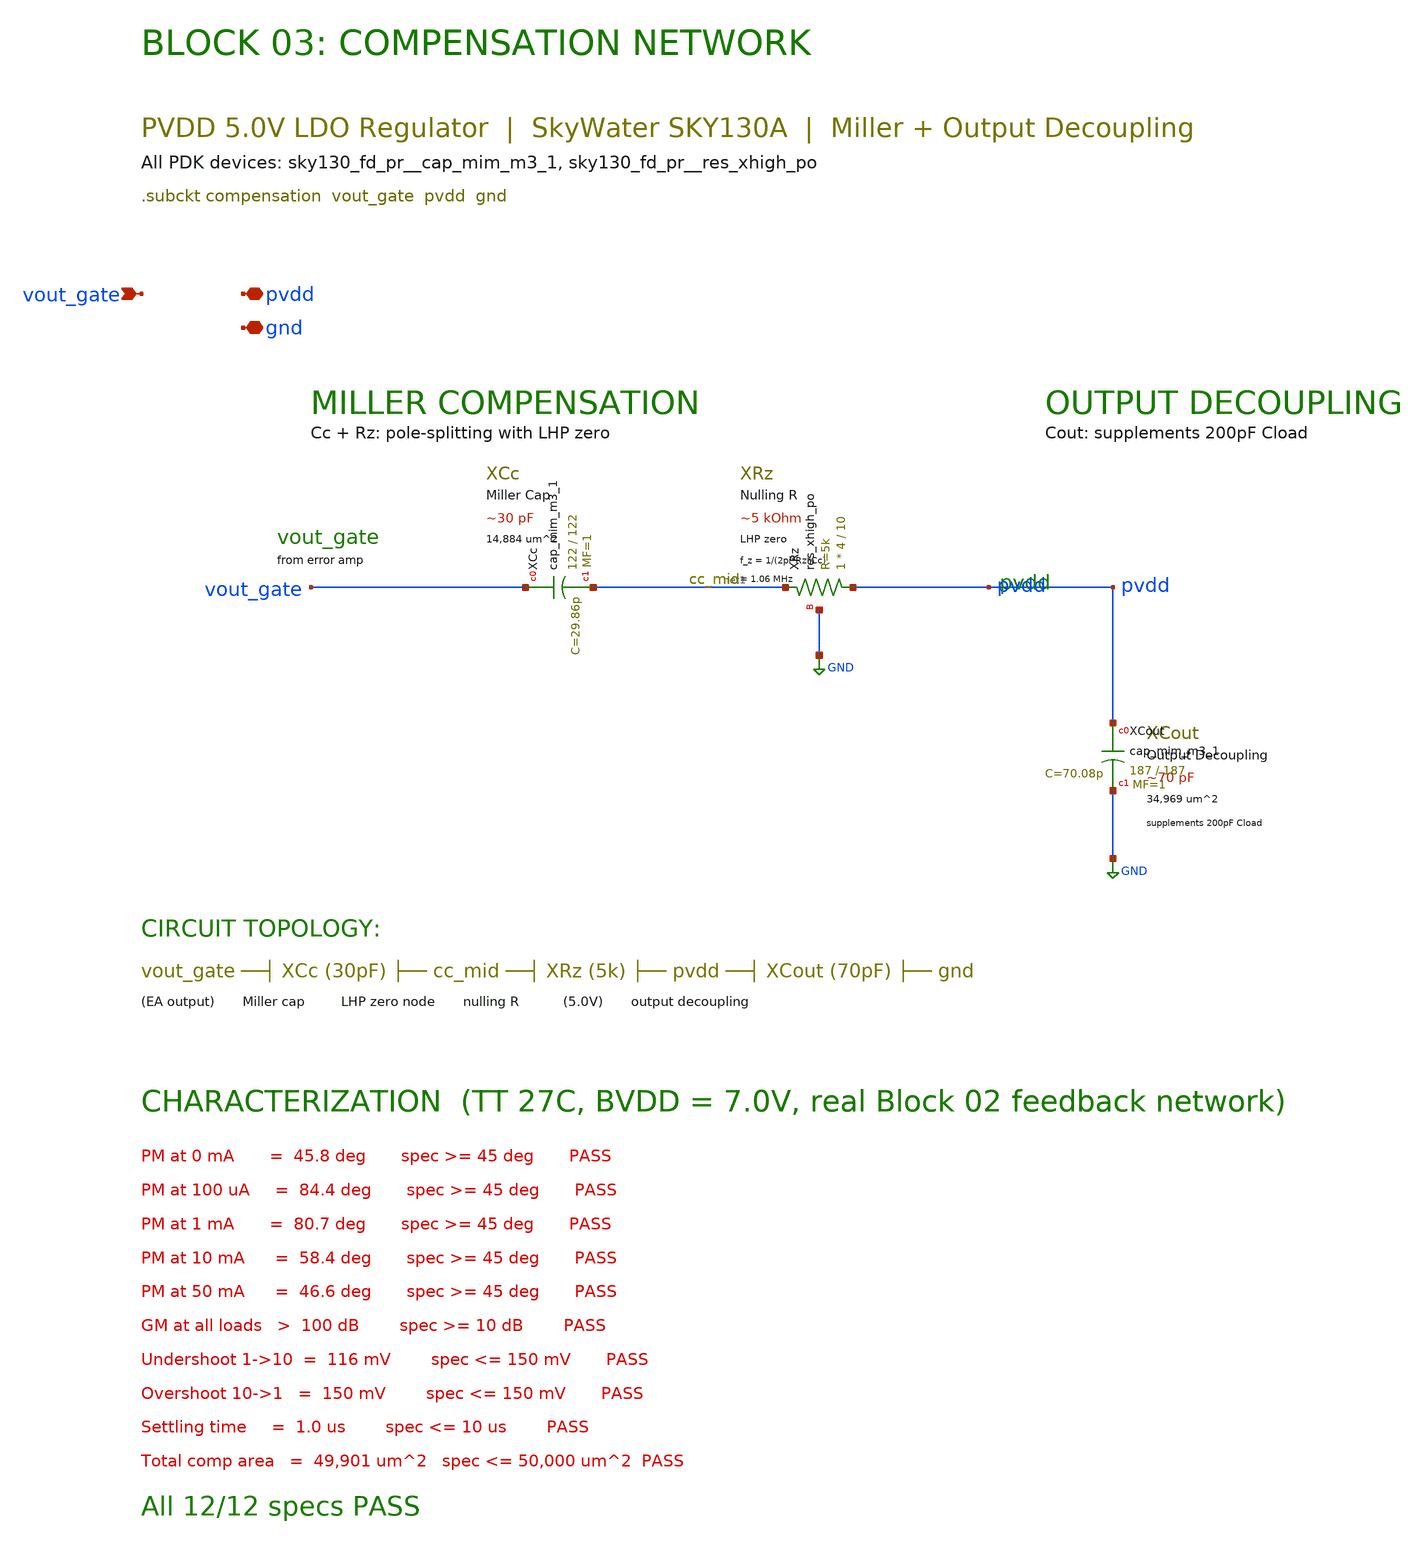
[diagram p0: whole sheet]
** sch_path: pvdd_regulator/03_compensation/compensation.sch
**.subckt compensation vout_gate pvdd gnd
*.ipin vout_gate
*.iopin pvdd
*.iopin gnd
XXCc vout_gate net1 sky130_fd_pr__cap_mim_m3_1 W=122 L=122 MF=1 m=1
XXRz pvdd net1 GND sky130_fd_pr__res_xhigh_po W=4 L=10 mult=1 m=1
XXCout pvdd GND sky130_fd_pr__cap_mim_m3_1 W=187 L=187 MF=1 m=1
**.ends
.GLOBAL GND
.end
